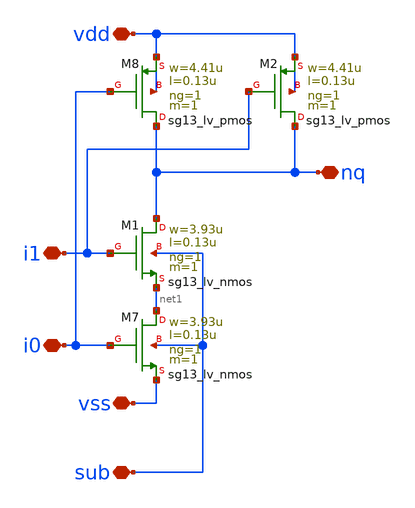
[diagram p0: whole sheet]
** sch_path: libs.tech/xschem/hm_stdcells/sg13g2_io_nand2_x1_noptap.sch
**.subckt sg13g2_io_nand2_x1_noptap vss nq i0 vdd sub i1
*.iopin vss
*.iopin nq
*.iopin i0
*.iopin vdd
*.iopin sub
*.iopin i1
XM7 net1 i0 vss sub sg13_lv_nmos w=3.93u l=0.13u ng=1 m=1 mm_ok=1
XM8 nq i0 vdd vdd sg13_lv_pmos w=4.41u l=0.13u ng=1 m=1 mm_ok=1
XM2 nq i1 vdd vdd sg13_lv_pmos w=4.41u l=0.13u ng=1 m=1 mm_ok=1
XM1 nq i1 net1 sub sg13_lv_nmos w=3.93u l=0.13u ng=1 m=1 mm_ok=1
**.ends
.end
